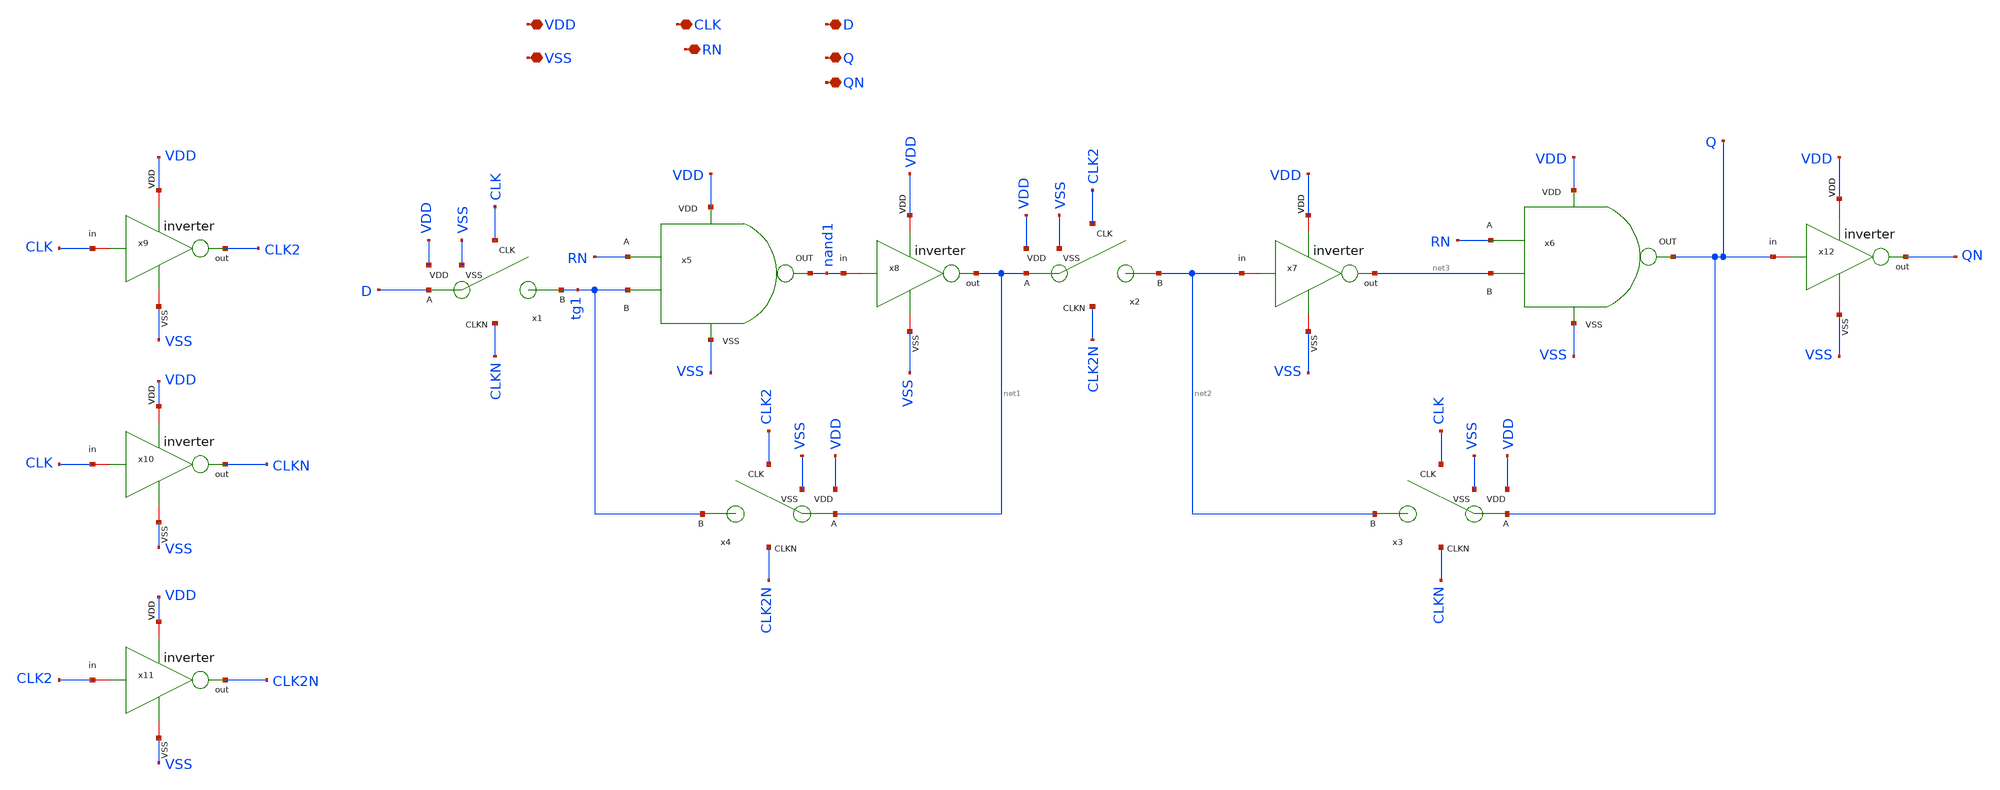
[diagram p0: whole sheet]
** sch_path: designs/sar_adc/digital/flip_flop/xschem/FF_D.sch
**.subckt FF_D VDD VSS CLK D RN Q QN
*.iopin VDD
*.iopin VSS
*.iopin CLK
*.iopin D
*.iopin RN
*.iopin Q
*.iopin QN
x1 CLK D VDD tg1 CLKN VSS TG
x2 CLK2 net1 VDD net2 CLK2N VSS TG
x3 CLK Q VDD net2 CLKN VSS TG
x4 CLK2 net1 VDD tg1 CLK2N VSS TG
x5 VDD VSS RN tg1 nand1 NAND
x6 VDD VSS RN net3 Q NAND
x8 VDD nand1 net1 VSS inverter
x9 VDD CLK CLK2 VSS inverter
x7 VDD net2 net3 VSS inverter
x10 VDD CLK CLKN VSS inverter
x11 VDD CLK2 CLK2N VSS inverter
x12 VDD Q QN VSS inverter
**.ends

* expanding   symbol:  designs/sar_adc/digital/TG/xschem/TG.sym # of pins=6
** sym_path: designs/sar_adc/digital/TG/xschem/TG.sym
** sch_path: designs/sar_adc/digital/TG/xschem/TG.sch
.subckt TG CLK A VDD B CLKN VSS
*.iopin VDD
*.iopin VSS
*.ipin CLK
*.ipin CLKN
*.iopin A
*.iopin B
XM1 A CLK B VSS nfet_03v3 L=0.28u W=0.22u nf=1 ad='int((nf+1)/2) * W/nf * 0.18u' as='int((nf+2)/2) * W/nf * 0.18u'
+ pd='2*int((nf+1)/2) * (W/nf + 0.18u)' ps='2*int((nf+2)/2) * (W/nf + 0.18u)' nrd='0.18u / W' nrs='0.18u / W'
+ sa=0 sb=0 sd=0 m=1
XM2 A CLKN B VDD pfet_03v3 L=0.28u W=0.22u nf=1 ad='int((nf+1)/2) * W/nf * 0.18u' as='int((nf+2)/2) * W/nf * 0.18u'
+ pd='2*int((nf+1)/2) * (W/nf + 0.18u)' ps='2*int((nf+2)/2) * (W/nf + 0.18u)' nrd='0.18u / W' nrs='0.18u / W'
+ sa=0 sb=0 sd=0 m=1
.ends


* expanding   symbol:  designs/sar_adc/digital/NAND/xschem/NAND.sym # of pins=5
** sym_path: designs/sar_adc/digital/NAND/xschem/NAND.sym
** sch_path: designs/sar_adc/digital/NAND/xschem/NAND.sch
.subckt NAND VDD VSS A B out
*.iopin VDD
*.iopin A
*.iopin B
*.iopin out
*.iopin VSS
xINVA VDD net1 net2 VSS inverter
xINVB[2] VDD net2 out VSS inverter
xINVB[1] VDD net2 out VSS inverter
xINVB[0] VDD net2 out VSS inverter
XM2 net1 A VDD VDD pfet_03v3 L=0.28u W=0.5u nf=1 ad='int((nf+1)/2) * W/nf * 0.18u' as='int((nf+2)/2) * W/nf * 0.18u'
+ pd='2*int((nf+1)/2) * (W/nf + 0.18u)' ps='2*int((nf+2)/2) * (W/nf + 0.18u)' nrd='0.18u / W' nrs='0.18u / W'
+ sa=0 sb=0 sd=0 m=2
XM1 net1 A net3 VSS nfet_03v3 L=0.28u W=0.5u nf=1 ad='int((nf+1)/2) * W/nf * 0.18u' as='int((nf+2)/2) * W/nf * 0.18u'
+ pd='2*int((nf+1)/2) * (W/nf + 0.18u)' ps='2*int((nf+2)/2) * (W/nf + 0.18u)' nrd='0.18u / W' nrs='0.18u / W'
+ sa=0 sb=0 sd=0 m=1
XM3 net1 B VDD VDD pfet_03v3 L=0.28u W=0.5u nf=1 ad='int((nf+1)/2) * W/nf * 0.18u' as='int((nf+2)/2) * W/nf * 0.18u'
+ pd='2*int((nf+1)/2) * (W/nf + 0.18u)' ps='2*int((nf+2)/2) * (W/nf + 0.18u)' nrd='0.18u / W' nrs='0.18u / W'
+ sa=0 sb=0 sd=0 m=2
XM4 net3 B VSS VSS nfet_03v3 L=0.28u W=0.5u nf=1 ad='int((nf+1)/2) * W/nf * 0.18u' as='int((nf+2)/2) * W/nf * 0.18u'
+ pd='2*int((nf+1)/2) * (W/nf + 0.18u)' ps='2*int((nf+2)/2) * (W/nf + 0.18u)' nrd='0.18u / W' nrs='0.18u / W'
+ sa=0 sb=0 sd=0 m=1
.ends


* expanding   symbol:  designs/sar_adc/digital/inverter/xschem/inverter.sym # of pins=6
** sym_path: designs/sar_adc/digital/inverter/xschem/inverter.sym
** sch_path: designs/sar_adc/digital/inverter/xschem/inverter.sch
.subckt inverter VDD in out VSS
*.opin out
*.iopin in
*.iopin VDD
*.iopin VSS
XM1 out in VSS VSS nfet_03v3 L=0.28u W=1u nf=1 ad='int((nf+1)/2) * W/nf * 0.18u' as='int((nf+2)/2) * W/nf * 0.18u'
+ pd='2*int((nf+1)/2) * (W/nf + 0.18u)' ps='2*int((nf+2)/2) * (W/nf + 0.18u)' nrd='0.18u / W' nrs='0.18u / W'
+ sa=0 sb=0 sd=0 m=1
XM2 out in VDD VDD pfet_03v3 L=0.28u W=3u nf=1 ad='int((nf+1)/2) * W/nf * 0.18u' as='int((nf+2)/2) * W/nf * 0.18u'
+ pd='2*int((nf+1)/2) * (W/nf + 0.18u)' ps='2*int((nf+2)/2) * (W/nf + 0.18u)' nrd='0.18u / W' nrs='0.18u / W'
+ sa=0 sb=0 sd=0 m=1
.ends

.end
